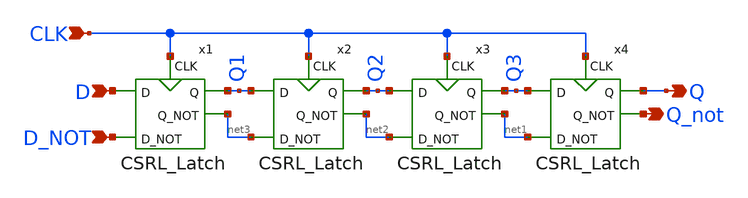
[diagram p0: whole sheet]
** sch_path: miniproject2/4BIT_SHIFT_REGISTER.sch
**.subckt 4BIT_SHIFT_REGISTER Q Q_not D D_NOT CLK
*.opin Q
*.opin Q_not
*.ipin D
*.ipin D_NOT
*.ipin CLK
x1 D Q1 D_NOT net3 CLK CSRL_Latch
x2 Q1 Q2 net3 net2 CLK CSRL_Latch
x3 Q2 Q3 net2 net1 CLK CSRL_Latch
x4 Q3 Q net1 Q_not CLK CSRL_Latch
**.ends

* expanding   symbol:  /home/lxbtlr/MAD/miniproject2/CSRL_Latch.sym # of pins=5
** sym_path: miniproject2/CSRL_Latch.sym
** sch_path: miniproject2/CSRL_Latch.sch
.subckt CSRL_Latch D Q D_NOT Q_NOT CLK
*.ipin D
*.ipin D_NOT
*.opin Q
*.opin Q_NOT
*.ipin CLK
XQ8 net2 net3 VDD VDD sky130_fd_pr__pfet_01v8 L=0.15 W=1 nf=1 ad='int((nf+1)/2) * W/nf * 0.29' as='int((nf+2)/2) * W/nf * 0.29'
+ pd='2*int((nf+1)/2) * (W/nf + 0.29)' ps='2*int((nf+2)/2) * (W/nf + 0.29)' nrd='0.29 / W' nrs='0.29 / W'
+ sa=0 sb=0 sd=0 mult=1 m=1
XQ9 VDD net2 net3 VDD sky130_fd_pr__pfet_01v8 L=0.15 W=1 nf=1 ad='int((nf+1)/2) * W/nf * 0.29' as='int((nf+2)/2) * W/nf * 0.29'
+ pd='2*int((nf+1)/2) * (W/nf + 0.29)' ps='2*int((nf+2)/2) * (W/nf + 0.29)' nrd='0.29 / W' nrs='0.29 / W'
+ sa=0 sb=0 sd=0 mult=1 m=1
XQ1 net3 CLK D VDD sky130_fd_pr__pfet_01v8 L=0.15 W=1 nf=1 ad='int((nf+1)/2) * W/nf * 0.29' as='int((nf+2)/2) * W/nf * 0.29'
+ pd='2*int((nf+1)/2) * (W/nf + 0.29)' ps='2*int((nf+2)/2) * (W/nf + 0.29)' nrd='0.29 / W' nrs='0.29 / W'
+ sa=0 sb=0 sd=0 mult=1 m=1
XQ2 net2 CLK D_NOT VDD sky130_fd_pr__pfet_01v8 L=0.15 W=1 nf=1 ad='int((nf+1)/2) * W/nf * 0.29' as='int((nf+2)/2) * W/nf * 0.29'
+ pd='2*int((nf+1)/2) * (W/nf + 0.29)' ps='2*int((nf+2)/2) * (W/nf + 0.29)' nrd='0.29 / W' nrs='0.29 / W'
+ sa=0 sb=0 sd=0 mult=1 m=1
XQ5 net1 CLK GND GND sky130_fd_pr__nfet_01v8 L=0.15 W=4 nf=1 ad='int((nf+1)/2) * W/nf * 0.29' as='int((nf+2)/2) * W/nf * 0.29'
+ pd='2*int((nf+1)/2) * (W/nf + 0.29)' ps='2*int((nf+2)/2) * (W/nf + 0.29)' nrd='0.29 / W' nrs='0.29 / W'
+ sa=0 sb=0 sd=0 mult=1 m=1
XQ4 Q_NOT CLK net2 GND sky130_fd_pr__nfet_01v8 L=0.15 W=1 nf=1 ad='int((nf+1)/2) * W/nf * 0.29' as='int((nf+2)/2) * W/nf * 0.29'
+ pd='2*int((nf+1)/2) * (W/nf + 0.29)' ps='2*int((nf+2)/2) * (W/nf + 0.29)' nrd='0.29 / W' nrs='0.29 / W'
+ sa=0 sb=0 sd=0 mult=1 m=1
XQ3 Q CLK net3 GND sky130_fd_pr__nfet_01v8 L=0.15 W=1 nf=1 ad='int((nf+1)/2) * W/nf * 0.29' as='int((nf+2)/2) * W/nf * 0.29'
+ pd='2*int((nf+1)/2) * (W/nf + 0.29)' ps='2*int((nf+2)/2) * (W/nf + 0.29)' nrd='0.29 / W' nrs='0.29 / W'
+ sa=0 sb=0 sd=0 mult=1 m=1
XQ6 net2 net3 net1 GND sky130_fd_pr__nfet_01v8 L=0.15 W=1 nf=1 ad='int((nf+1)/2) * W/nf * 0.29' as='int((nf+2)/2) * W/nf * 0.29'
+ pd='2*int((nf+1)/2) * (W/nf + 0.29)' ps='2*int((nf+2)/2) * (W/nf + 0.29)' nrd='0.29 / W' nrs='0.29 / W'
+ sa=0 sb=0 sd=0 mult=1 m=1
XQ7 net1 net2 net3 GND sky130_fd_pr__nfet_01v8 L=0.15 W=1 nf=1 ad='int((nf+1)/2) * W/nf * 0.29' as='int((nf+2)/2) * W/nf * 0.29'
+ pd='2*int((nf+1)/2) * (W/nf + 0.29)' ps='2*int((nf+2)/2) * (W/nf + 0.29)' nrd='0.29 / W' nrs='0.29 / W'
+ sa=0 sb=0 sd=0 mult=1 m=1
XQ13 Q_NOT Q GND GND sky130_fd_pr__nfet_01v8 L=0.15 W=1 nf=1 ad='int((nf+1)/2) * W/nf * 0.29' as='int((nf+2)/2) * W/nf * 0.29'
+ pd='2*int((nf+1)/2) * (W/nf + 0.29)' ps='2*int((nf+2)/2) * (W/nf + 0.29)' nrd='0.29 / W' nrs='0.29 / W'
+ sa=0 sb=0 sd=0 mult=1 m=1
XQ14 GND Q_NOT Q GND sky130_fd_pr__nfet_01v8 L=0.15 W=1 nf=1 ad='int((nf+1)/2) * W/nf * 0.29' as='int((nf+2)/2) * W/nf * 0.29'
+ pd='2*int((nf+1)/2) * (W/nf + 0.29)' ps='2*int((nf+2)/2) * (W/nf + 0.29)' nrd='0.29 / W' nrs='0.29 / W'
+ sa=0 sb=0 sd=0 mult=1 m=1
XQ11 Q_NOT Q net4 VDD sky130_fd_pr__pfet_01v8 L=0.15 W=1 nf=1 ad='int((nf+1)/2) * W/nf * 0.29' as='int((nf+2)/2) * W/nf * 0.29'
+ pd='2*int((nf+1)/2) * (W/nf + 0.29)' ps='2*int((nf+2)/2) * (W/nf + 0.29)' nrd='0.29 / W' nrs='0.29 / W'
+ sa=0 sb=0 sd=0 mult=1 m=1
XQ12 net4 Q_NOT Q VDD sky130_fd_pr__pfet_01v8 L=0.15 W=1 nf=1 ad='int((nf+1)/2) * W/nf * 0.29' as='int((nf+2)/2) * W/nf * 0.29'
+ pd='2*int((nf+1)/2) * (W/nf + 0.29)' ps='2*int((nf+2)/2) * (W/nf + 0.29)' nrd='0.29 / W' nrs='0.29 / W'
+ sa=0 sb=0 sd=0 mult=1 m=1
XQ10 net4 CLK VDD VDD sky130_fd_pr__pfet_01v8 L=0.15 W=4 nf=1 ad='int((nf+1)/2) * W/nf * 0.29' as='int((nf+2)/2) * W/nf * 0.29'
+ pd='2*int((nf+1)/2) * (W/nf + 0.29)' ps='2*int((nf+2)/2) * (W/nf + 0.29)' nrd='0.29 / W' nrs='0.29 / W'
+ sa=0 sb=0 sd=0 mult=1 m=1
.ends

.GLOBAL GND
.GLOBAL VDD
.end
